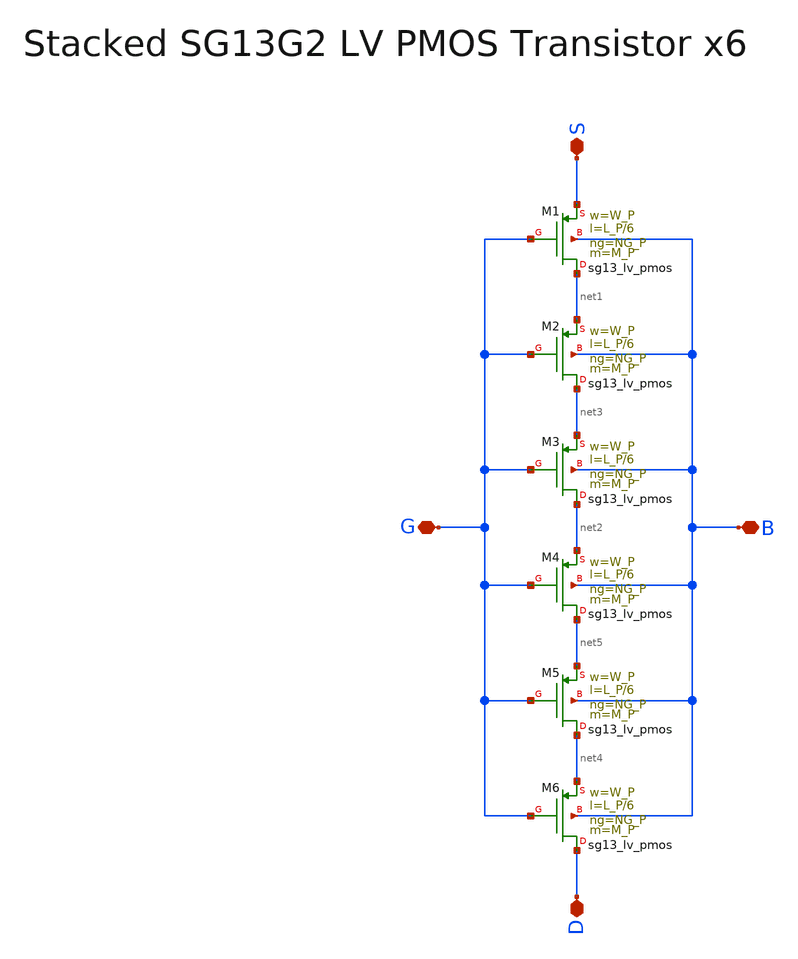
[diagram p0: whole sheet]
** sch_path: SG13G2_ATBS-ADC-main/xschem/stacked_transistors/sg13g2_lv_pmos_stacked/sg13g2_lv_pmos_stacked_x6.sch
**.subckt sg13g2_lv_pmos_stacked_x6 D S G B
*.iopin D
*.iopin S
*.iopin G
*.iopin B
XM1 net1 G S B sg13_lv_pmos w=W_P l=L_P/6 ng=NG_P m=M_P mm_ok=1
XM2 net3 G net1 B sg13_lv_pmos w=W_P l=L_P/6 ng=NG_P m=M_P mm_ok=1
XM3 net2 G net3 B sg13_lv_pmos w=W_P l=L_P/6 ng=NG_P m=M_P mm_ok=1
XM4 net5 G net2 B sg13_lv_pmos w=W_P l=L_P/6 ng=NG_P m=M_P mm_ok=1
XM5 net4 G net5 B sg13_lv_pmos w=W_P l=L_P/6 ng=NG_P m=M_P mm_ok=1
XM6 D G net4 B sg13_lv_pmos w=W_P l=L_P/6 ng=NG_P m=M_P mm_ok=1
**.ends
.end
